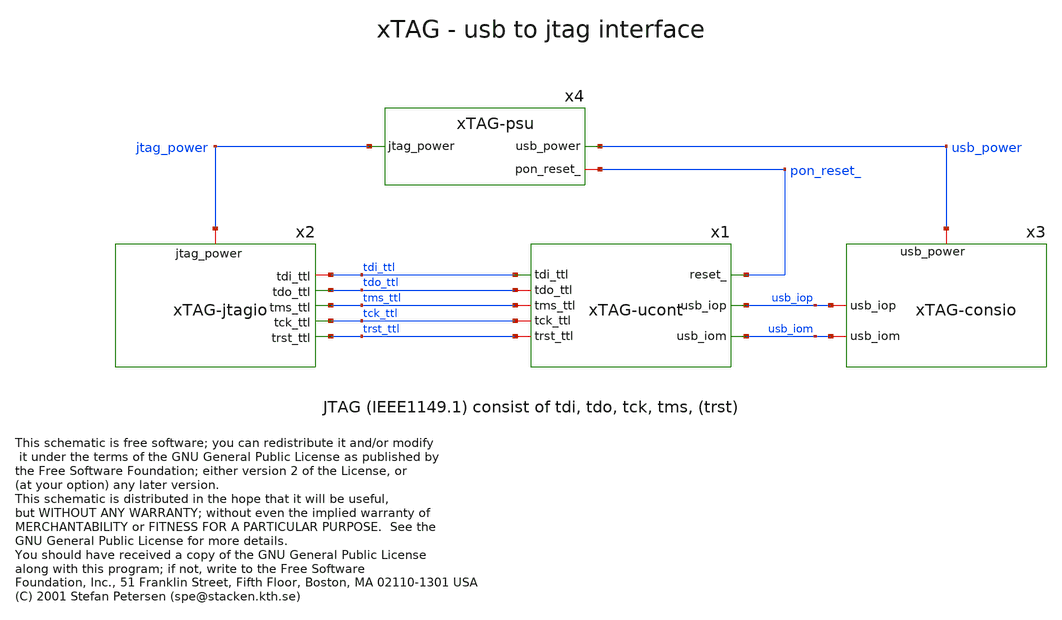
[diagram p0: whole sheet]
** sch_path: xschem_libs_newsym/xTAG/xTAG/schematic/xTAG.sch
* Copyright (C) 1998-2024 Stefan Frederik Schippers
* This program is free software; you can redistribute it and/or modify
* it under the terms of the GNU General Public License as published by
* the Free Software Foundation; either version 2 of the License, or
* (at your option) any later version.
* This program is distributed in the hope that it will be useful,
* but WITHOUT ANY WARRANTY; without even the implied warranty of
* MERCHANTABILITY or FITNESS FOR A PARTICULAR PURPOSE.  See the
* GNU General Public License for more details.
* You should have received a copy of the GNU General Public License
* along with this program; if not, write to the Free Software
* This schematic is free software; you can redistribute it and/or modify
* (C) 2001 Stefan Petersen (spe@stacken.kth.se)
**.subckt xTAG
x4 usb_power pon_reset_ jtag_power xTAG-psu
x2 jtag_power tdi_ttl tdo_ttl tms_ttl tck_ttl trst_ttl xTAG-jtagio
x1 tdi_ttl tdo_ttl tms_ttl tck_ttl trst_ttl pon_reset_ usb_iop usb_iom xTAG-ucont
x3 usb_power usb_iop usb_iom xTAG-consio
**.ends
.end
